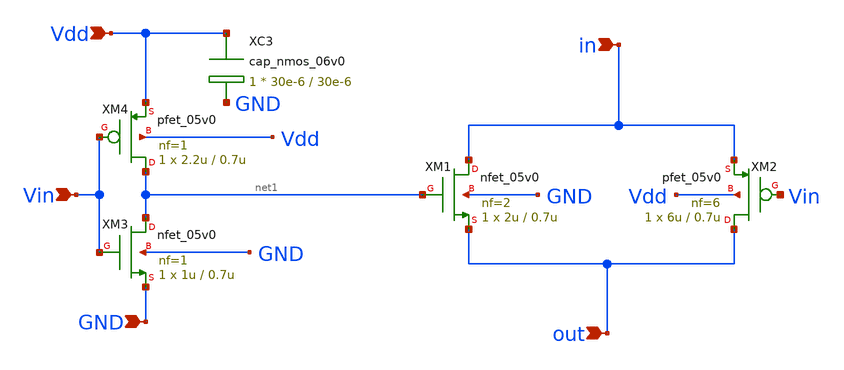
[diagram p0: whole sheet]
** sch_path: MG_switch/cmos_neg_switch.sch
**.subckt cmos_neg_switch Vdd Vin in out GND
*.ipin Vdd
*.ipin Vin
*.ipin in
*.ipin out
*.ipin GND
XM1 in net1 out GND nfet_05v0 L=0.7u W=2u nf=2 ad='int((nf+1)/2) * W/nf * 0.18u' as='int((nf+2)/2) * W/nf * 0.18u'
+ pd='2*int((nf+1)/2) * (W/nf + 0.18u)' ps='2*int((nf+2)/2) * (W/nf + 0.18u)' nrd='0.18u / W' nrs='0.18u / W'
+ sa=0 sb=0 sd=0 m=1
XM2 out Vin in Vdd pfet_05v0 L=0.7u W=6u nf=6 ad='int((nf+1)/2) * W/nf * 0.18u' as='int((nf+2)/2) * W/nf * 0.18u'
+ pd='2*int((nf+1)/2) * (W/nf + 0.18u)' ps='2*int((nf+2)/2) * (W/nf + 0.18u)' nrd='0.18u / W' nrs='0.18u / W'
+ sa=0 sb=0 sd=0 m=1
XM3 net1 Vin GND GND nfet_05v0 L=0.7u W=1u nf=1 ad='int((nf+1)/2) * W/nf * 0.18u' as='int((nf+2)/2) * W/nf * 0.18u'
+ pd='2*int((nf+1)/2) * (W/nf + 0.18u)' ps='2*int((nf+2)/2) * (W/nf + 0.18u)' nrd='0.18u / W' nrs='0.18u / W'
+ sa=0 sb=0 sd=0 m=1
XM4 net1 Vin Vdd Vdd pfet_05v0 L=0.7u W=2.2u nf=1 ad='int((nf+1)/2) * W/nf * 0.18u' as='int((nf+2)/2) * W/nf * 0.18u'
+ pd='2*int((nf+1)/2) * (W/nf + 0.18u)' ps='2*int((nf+2)/2) * (W/nf + 0.18u)' nrd='0.18u / W' nrs='0.18u / W'
+ sa=0 sb=0 sd=0 m=1
XC3 Vdd GND cap_nmos_06v0 c_width=30e-6 c_length=30e-6 m=1
**.ends
.end
